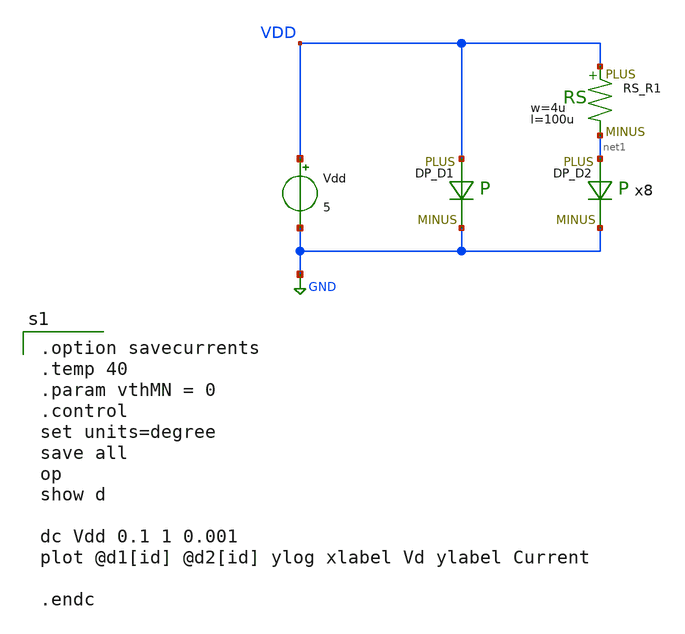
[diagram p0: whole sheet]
** sch_path: IO_202604/07/xschem/test_diode.sch
**.subckt test_diode
Vdd VDD GND 5
D1 VDD GND DP m=1
D2 net1 GND DP m=8
XR1 VDD net1 F_RS w=4u R=1 l=100u tc1=0 tc2=0
**** begin user architecture code
 .include $::LIB/../ip62_models

.option savecurrents
.temp 40
.param vthMN = 0
.control
set units=degree
save all
op
show d

dc Vdd 0.1 1 0.001
plot @d1[id] @d2[id] ylog xlabel Vd ylabel Current

.endc

**** end user architecture code
**.ends
.GLOBAL GND
.end
